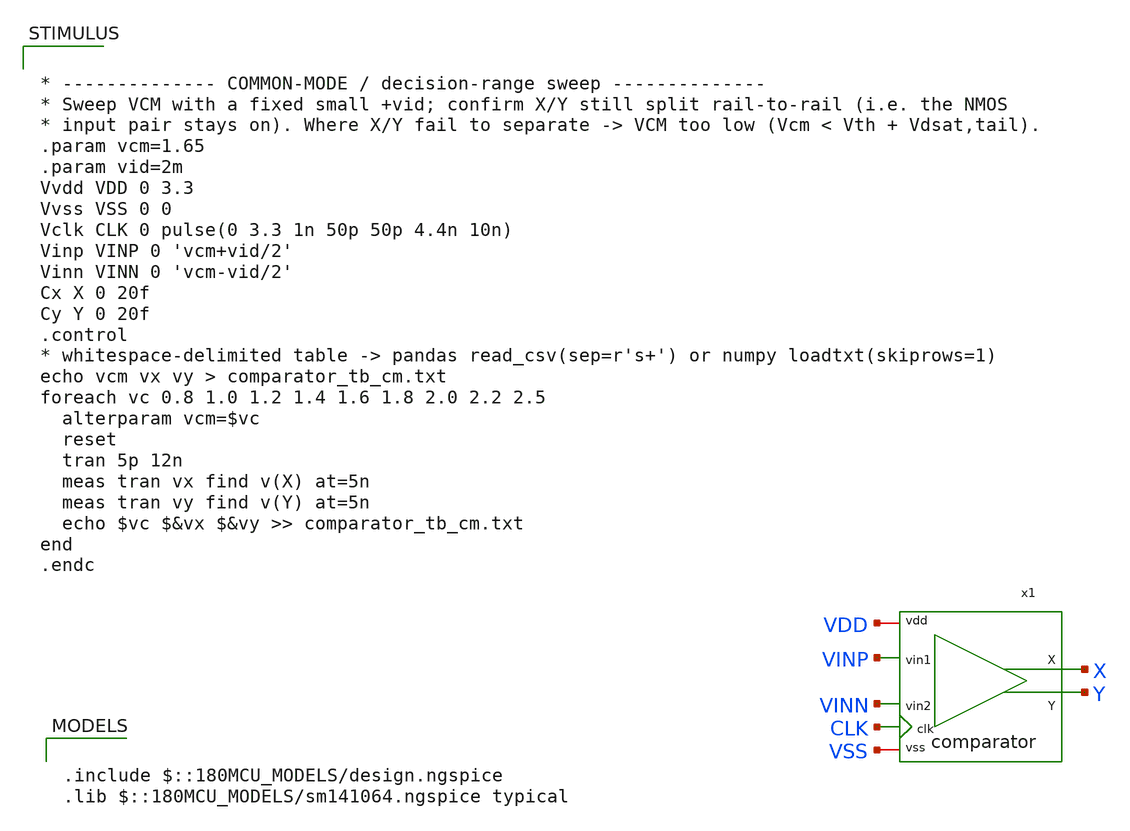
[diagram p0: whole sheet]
** sch_path: designs/libs/core_analog/saradc/tb/comparator_tb_cm.sch
**.subckt comparator_tb_cm
x1 VDD VSS X VINP Y VINN CLK comparator
**** begin user architecture code

.include $::180MCU_MODELS/design.ngspice
.lib $::180MCU_MODELS/sm141064.ngspice typical



* -------------- COMMON-MODE / decision-range sweep --------------
* Sweep VCM with a fixed small +vid; confirm X/Y still split rail-to-rail (i.e. the NMOS
* input pair stays on). Where X/Y fail to separate -> VCM too low (Vcm < Vth + Vdsat,tail).
.param vcm=1.65
.param vid=2m
Vvdd VDD 0 3.3
Vvss VSS 0 0
Vclk CLK 0 pulse(0 3.3 1n 50p 50p 4.4n 10n)
Vinp VINP 0 'vcm+vid/2'
Vinn VINN 0 'vcm-vid/2'
Cx X 0 20f
Cy Y 0 20f
.control
* whitespace-delimited table -> pandas read_csv(sep=r's+') or numpy loadtxt(skiprows=1)
echo vcm vx vy > comparator_tb_cm.txt
foreach vc 0.8 1.0 1.2 1.4 1.6 1.8 2.0 2.2 2.5
  alterparam vcm=$vc
  reset
  tran 5p 12n
  meas tran vx find v(X) at=5n
  meas tran vy find v(Y) at=5n
  echo $vc $&vx $&vy >> comparator_tb_cm.txt
end
.endc


**** end user architecture code
**.ends

* expanding   symbol:  comparator.sym # of pins=7
** sym_path: designs/libs/core_analog/saradc/comparator.sym
** sch_path: designs/libs/core_analog/saradc/comparator.sch
.subckt comparator vdd vss X vin1 Y vin2 clk
*.iopin vdd
*.iopin vss
*.ipin vin1
*.ipin vin2
*.ipin clk
*.opin X
*.opin Y
XM1 P vin1 net1 vss nfet_03v3 L=0.5u W=4u nf=4 ad='int((nf+1)/2) * W/nf * 0.18u' as='int((nf+2)/2) * W/nf * 0.18u'
+ pd='2*int((nf+1)/2) * (W/nf + 0.18u)' ps='2*int((nf+2)/2) * (W/nf + 0.18u)' nrd='0.18u / W' nrs='0.18u / W'
+ sa=0 sb=0 sd=0 m=1
XM2 Q vin2 net1 vss nfet_03v3 L=0.5u W=4u nf=4 ad='int((nf+1)/2) * W/nf * 0.18u' as='int((nf+2)/2) * W/nf * 0.18u'
+ pd='2*int((nf+1)/2) * (W/nf + 0.18u)' ps='2*int((nf+2)/2) * (W/nf + 0.18u)' nrd='0.18u / W' nrs='0.18u / W'
+ sa=0 sb=0 sd=0 m=1
XM3 X Y P vss nfet_03v3 L=0.28u W=2u nf=2 ad='int((nf+1)/2) * W/nf * 0.18u' as='int((nf+2)/2) * W/nf * 0.18u'
+ pd='2*int((nf+1)/2) * (W/nf + 0.18u)' ps='2*int((nf+2)/2) * (W/nf + 0.18u)' nrd='0.18u / W' nrs='0.18u / W'
+ sa=0 sb=0 sd=0 m=1
XM4 Y X Q vss nfet_03v3 L=0.28u W=2u nf=2 ad='int((nf+1)/2) * W/nf * 0.18u' as='int((nf+2)/2) * W/nf * 0.18u'
+ pd='2*int((nf+1)/2) * (W/nf + 0.18u)' ps='2*int((nf+2)/2) * (W/nf + 0.18u)' nrd='0.18u / W' nrs='0.18u / W'
+ sa=0 sb=0 sd=0 m=1
XM5 X Y vdd vdd pfet_03v3 L=0.28u W=6u nf=2 ad='int((nf+1)/2) * W/nf * 0.18u' as='int((nf+2)/2) * W/nf * 0.18u'
+ pd='2*int((nf+1)/2) * (W/nf + 0.18u)' ps='2*int((nf+2)/2) * (W/nf + 0.18u)' nrd='0.18u / W' nrs='0.18u / W'
+ sa=0 sb=0 sd=0 m=1
XM6 Y X vdd vdd pfet_03v3 L=0.28u W=6u nf=2 ad='int((nf+1)/2) * W/nf * 0.18u' as='int((nf+2)/2) * W/nf * 0.18u'
+ pd='2*int((nf+1)/2) * (W/nf + 0.18u)' ps='2*int((nf+2)/2) * (W/nf + 0.18u)' nrd='0.18u / W' nrs='0.18u / W'
+ sa=0 sb=0 sd=0 m=1
XM7 net1 clk vss vss nfet_03v3 L=0.28u W=6u nf=4 ad='int((nf+1)/2) * W/nf * 0.18u' as='int((nf+2)/2) * W/nf * 0.18u'
+ pd='2*int((nf+1)/2) * (W/nf + 0.18u)' ps='2*int((nf+2)/2) * (W/nf + 0.18u)' nrd='0.18u / W' nrs='0.18u / W'
+ sa=0 sb=0 sd=0 m=1
XM8 X clk vdd vdd pfet_03v3 L=0.28u W=2u nf=1 ad='int((nf+1)/2) * W/nf * 0.18u' as='int((nf+2)/2) * W/nf * 0.18u'
+ pd='2*int((nf+1)/2) * (W/nf + 0.18u)' ps='2*int((nf+2)/2) * (W/nf + 0.18u)' nrd='0.18u / W' nrs='0.18u / W'
+ sa=0 sb=0 sd=0 m=1
XM9 P clk vdd vdd pfet_03v3 L=0.28u W=2u nf=1 ad='int((nf+1)/2) * W/nf * 0.18u' as='int((nf+2)/2) * W/nf * 0.18u'
+ pd='2*int((nf+1)/2) * (W/nf + 0.18u)' ps='2*int((nf+2)/2) * (W/nf + 0.18u)' nrd='0.18u / W' nrs='0.18u / W'
+ sa=0 sb=0 sd=0 m=1
XM10 Y clk vdd vdd pfet_03v3 L=0.28u W=2u nf=1 ad='int((nf+1)/2) * W/nf * 0.18u' as='int((nf+2)/2) * W/nf * 0.18u'
+ pd='2*int((nf+1)/2) * (W/nf + 0.18u)' ps='2*int((nf+2)/2) * (W/nf + 0.18u)' nrd='0.18u / W' nrs='0.18u / W'
+ sa=0 sb=0 sd=0 m=1
XM11 Q clk vdd vdd pfet_03v3 L=0.28u W=2u nf=1 ad='int((nf+1)/2) * W/nf * 0.18u' as='int((nf+2)/2) * W/nf * 0.18u'
+ pd='2*int((nf+1)/2) * (W/nf + 0.18u)' ps='2*int((nf+2)/2) * (W/nf + 0.18u)' nrd='0.18u / W' nrs='0.18u / W'
+ sa=0 sb=0 sd=0 m=1
.ends

.end
